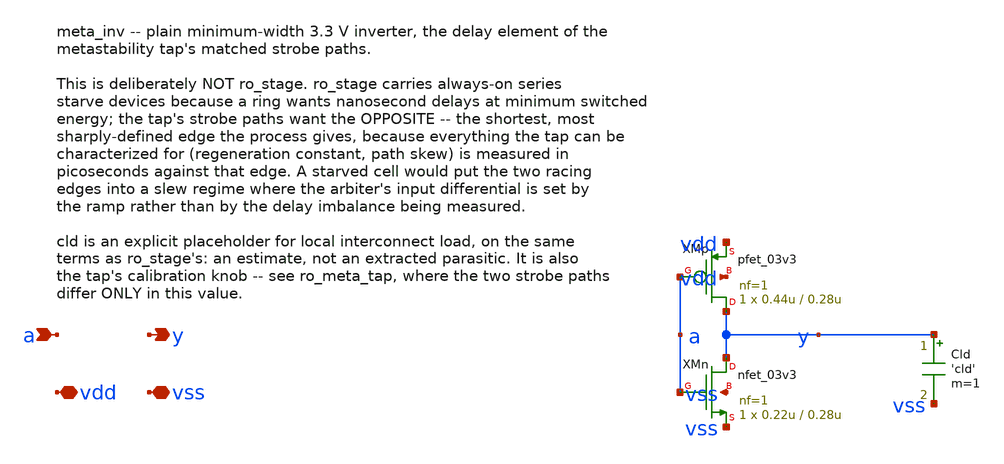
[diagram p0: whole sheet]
** sch_path: design/xschem/meta_inv.sch
**.subckt meta_inv a y vdd vss
*.ipin a
*.opin y
*.iopin vdd
*.iopin vss
XMp y a vdd vdd pfet_03v3 L=0.28u W=0.44u nf=1 ad='int((nf+1)/2) * W/nf * 0.18u' as='int((nf+2)/2) * W/nf * 0.18u'
+ pd='2*int((nf+1)/2) * (W/nf + 0.18u)' ps='2*int((nf+2)/2) * (W/nf + 0.18u)' nrd='0.18u / W' nrs='0.18u / W'
+ sa=0 sb=0 sd=0 m=1
XMn y a vss vss nfet_03v3 L=0.28u W=0.22u nf=1 ad='int((nf+1)/2) * W/nf * 0.18u' as='int((nf+2)/2) * W/nf * 0.18u'
+ pd='2*int((nf+1)/2) * (W/nf + 0.18u)' ps='2*int((nf+2)/2) * (W/nf + 0.18u)' nrd='0.18u / W' nrs='0.18u / W'
+ sa=0 sb=0 sd=0 m=1
Cld y vss 'cld' m=1
**.ends
.end
